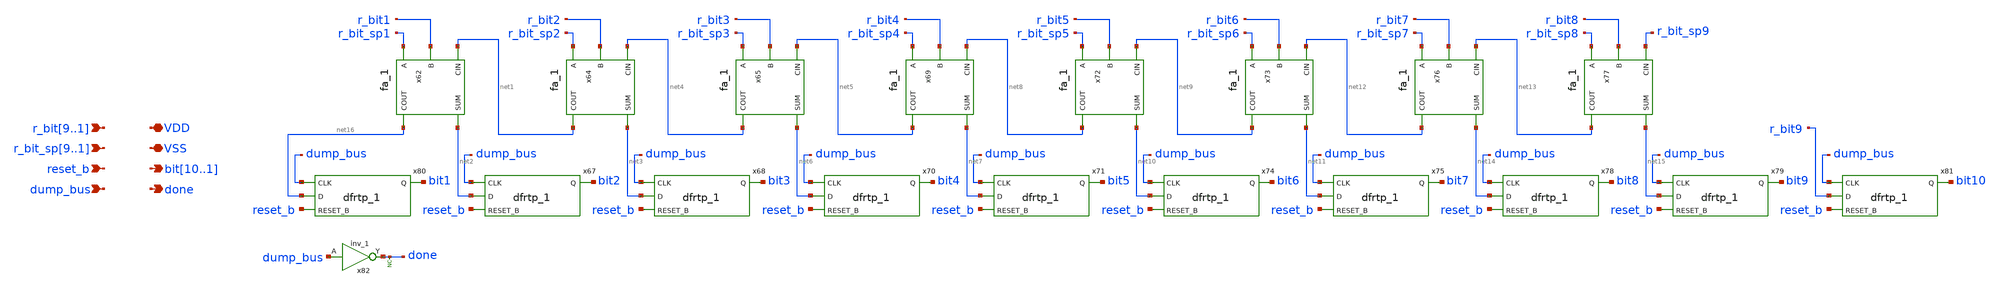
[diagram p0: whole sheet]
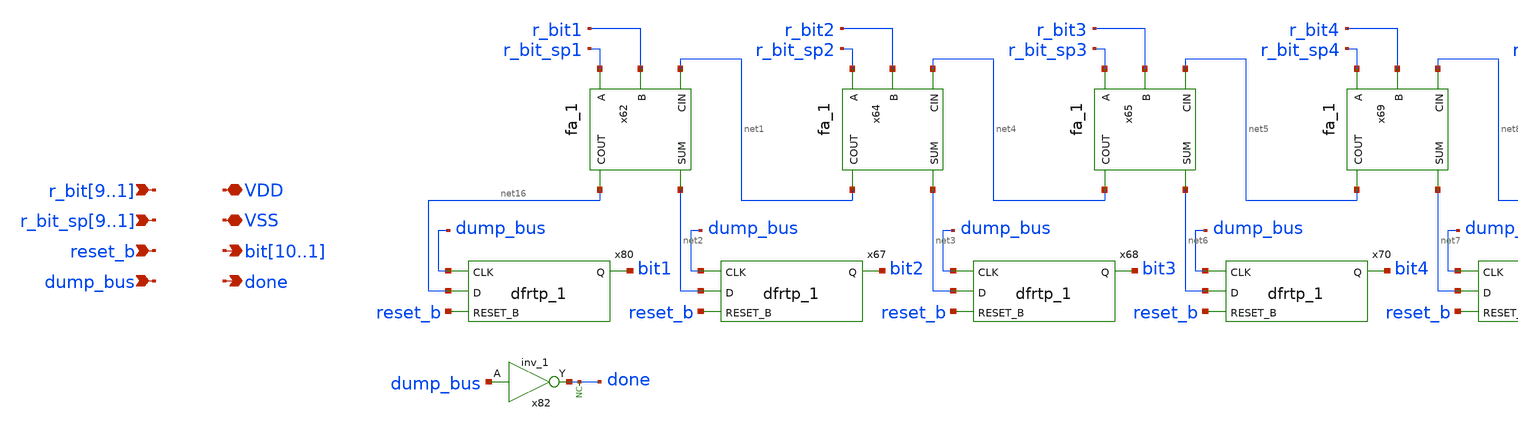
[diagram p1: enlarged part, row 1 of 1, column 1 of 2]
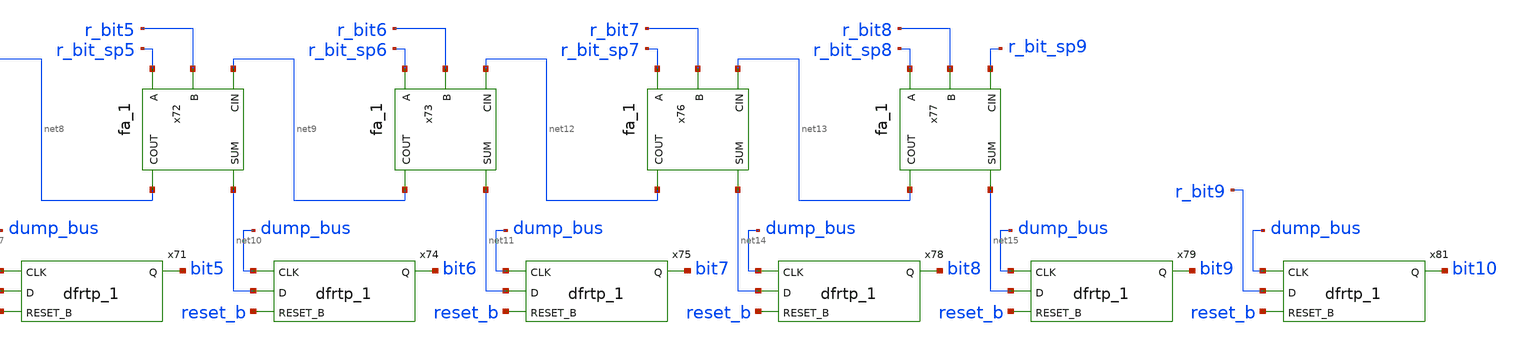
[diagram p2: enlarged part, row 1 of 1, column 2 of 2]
** sch_path: xschem/src/dec/dec.sch
**.subckt dec r_bit9,r_bit8,r_bit7,r_bit6,r_bit5,r_bit4,r_bit3,r_bit2,r_bit1 VDD
*+ bit10,bit9,bit8,bit7,bit6,bit5,bit4,bit3,bit2,bit1 VSS r_bit_sp9,r_bit_sp8,r_bit_sp7,r_bit_sp6,r_bit_sp5,r_bit_sp4,r_bit_sp3,r_bit_sp2,r_bit_sp1
*+ reset_b dump_bus done
*.ipin r_bit9,r_bit8,r_bit7,r_bit6,r_bit5,r_bit4,r_bit3,r_bit2,r_bit1
*.iopin VDD
*.opin bit10,bit9,bit8,bit7,bit6,bit5,bit4,bit3,bit2,bit1
*.iopin VSS
*.ipin r_bit_sp9,r_bit_sp8,r_bit_sp7,r_bit_sp6,r_bit_sp5,r_bit_sp4,r_bit_sp3,r_bit_sp2,r_bit_sp1
*.ipin reset_b
*.ipin dump_bus
*.opin done
x62 r_bit_sp1 r_bit1 net1 VSS VSS VDD VDD net16 net2 sky130_fd_sc_hd__fa_1
x64 r_bit_sp2 r_bit2 net4 VSS VSS VDD VDD net1 net3 sky130_fd_sc_hd__fa_1
x67 dump_bus net2 reset_b VSS VSS VDD VDD bit2 sky130_fd_sc_hd__dfrtp_1
x68 dump_bus net3 reset_b VSS VSS VDD VDD bit3 sky130_fd_sc_hd__dfrtp_1
x65 r_bit_sp3 r_bit3 net5 VSS VSS VDD VDD net4 net6 sky130_fd_sc_hd__fa_1
x69 r_bit_sp4 r_bit4 net8 VSS VSS VDD VDD net5 net7 sky130_fd_sc_hd__fa_1
x70 dump_bus net6 reset_b VSS VSS VDD VDD bit4 sky130_fd_sc_hd__dfrtp_1
x71 dump_bus net7 reset_b VSS VSS VDD VDD bit5 sky130_fd_sc_hd__dfrtp_1
x72 r_bit_sp5 r_bit5 net9 VSS VSS VDD VDD net8 net10 sky130_fd_sc_hd__fa_1
x73 r_bit_sp6 r_bit6 net12 VSS VSS VDD VDD net9 net11 sky130_fd_sc_hd__fa_1
x74 dump_bus net10 reset_b VSS VSS VDD VDD bit6 sky130_fd_sc_hd__dfrtp_1
x75 dump_bus net11 reset_b VSS VSS VDD VDD bit7 sky130_fd_sc_hd__dfrtp_1
x76 r_bit_sp7 r_bit7 net13 VSS VSS VDD VDD net12 net14 sky130_fd_sc_hd__fa_1
x77 r_bit_sp8 r_bit8 r_bit_sp9 VSS VSS VDD VDD net13 net15 sky130_fd_sc_hd__fa_1
x78 dump_bus net14 reset_b VSS VSS VDD VDD bit8 sky130_fd_sc_hd__dfrtp_1
x79 dump_bus net15 reset_b VSS VSS VDD VDD bit9 sky130_fd_sc_hd__dfrtp_1
x80 dump_bus net16 reset_b VSS VSS VDD VDD bit1 sky130_fd_sc_hd__dfrtp_1
x81 dump_bus r_bit9 reset_b VSS VSS VDD VDD bit10 sky130_fd_sc_hd__dfrtp_1
x82 dump_bus VSS VSS VDD VDD done sky130_fd_sc_hd__inv_1
* noconn done
**.ends
.end
